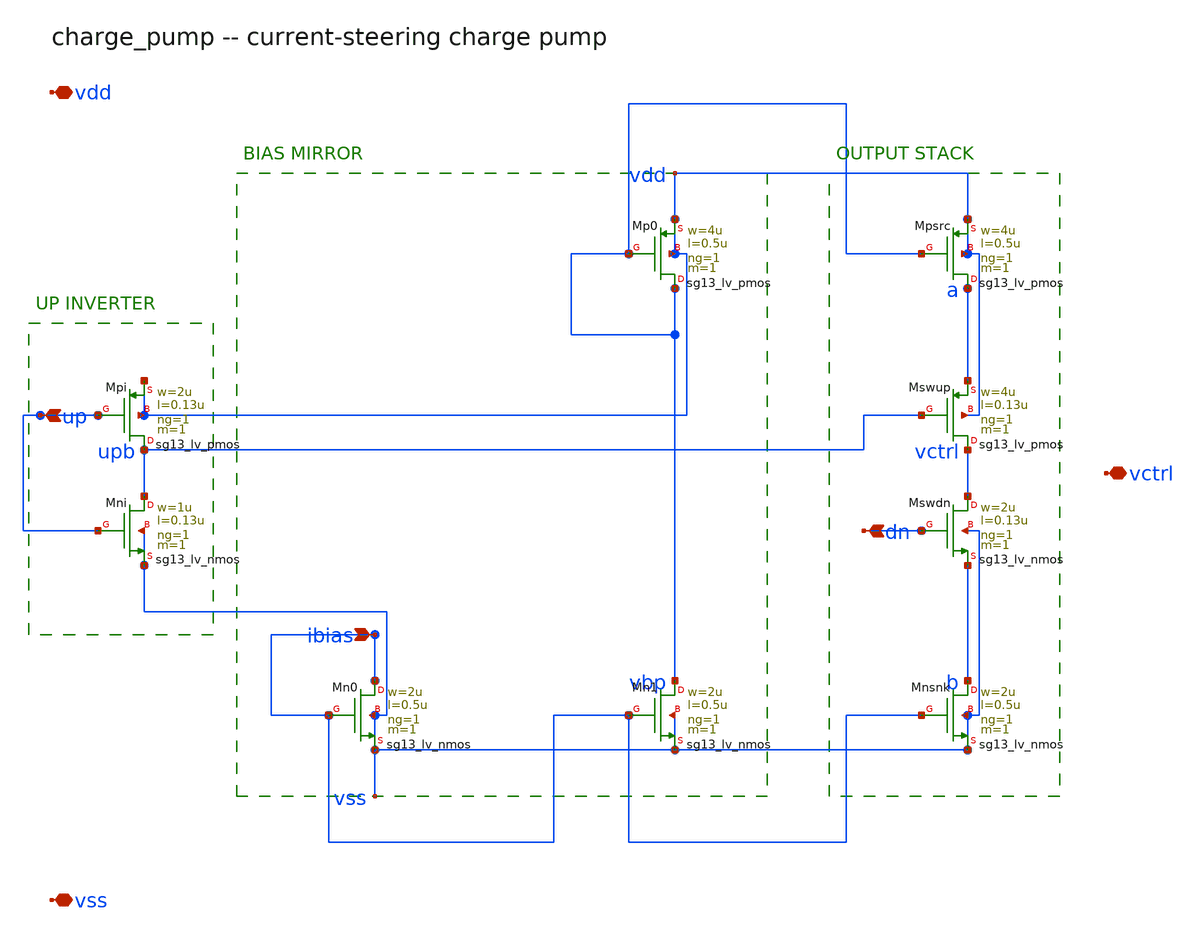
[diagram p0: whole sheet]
** sch_path: xschem/charge_pump_wired.sch
**.subckt charge_pump_wired up dn ibias vctrl vdd vss
*.ipin up
*.ipin dn
*.ipin ibias
*.iopin vctrl
*.iopin vdd
*.iopin vss
XMn0 ibias ibias vss vss sg13_lv_nmos w=2u l=0.5u ng=1 m=1 mm_ok=1
XMn1 vbp ibias vss vss sg13_lv_nmos w=2u l=0.5u ng=1 m=1 mm_ok=1
XMp0 vbp vbp vdd vdd sg13_lv_pmos w=4u l=0.5u ng=1 m=1 mm_ok=1
XMpsrc a vbp vdd vdd sg13_lv_pmos w=4u l=0.5u ng=1 m=1 mm_ok=1
XMnsnk b ibias vss vss sg13_lv_nmos w=2u l=0.5u ng=1 m=1 mm_ok=1
XMpi upb up vdd vdd sg13_lv_pmos w=2u l=0.13u ng=1 m=1 mm_ok=1
XMni upb up vss vss sg13_lv_nmos w=1u l=0.13u ng=1 m=1 mm_ok=1
XMswup vctrl upb a vdd sg13_lv_pmos w=4u l=0.13u ng=1 m=1 mm_ok=1
XMswdn vctrl dn b vss sg13_lv_nmos w=2u l=0.13u ng=1 m=1 mm_ok=1
**.ends
.end
